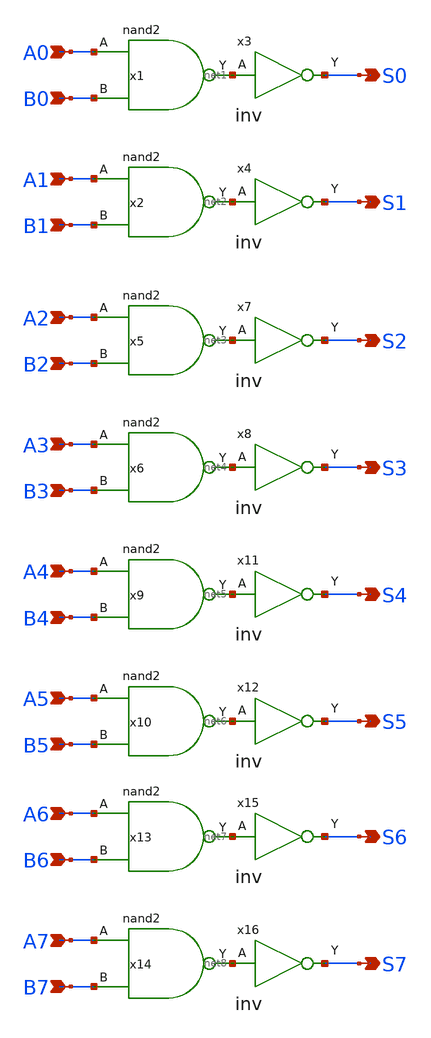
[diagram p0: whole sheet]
** sch_path: design/xschem/NAND/nand_8_bitwise.sch
**.subckt nand_8_bitwise S0 S1 S2 S3 S4 S5 S6 S7 A0 B0 A1 B1 A2 B2 A3 B3 A4 B4 A5 B5 A6 B6 A7 B7
*.opin S0
*.opin S1
*.opin S2
*.opin S3
*.opin S4
*.opin S5
*.opin S6
*.opin S7
*.ipin A0
*.ipin B0
*.ipin A1
*.ipin B1
*.ipin A2
*.ipin B2
*.ipin A3
*.ipin B3
*.ipin A4
*.ipin B4
*.ipin A5
*.ipin B5
*.ipin A6
*.ipin B6
*.ipin A7
*.ipin B7
x1 A0 B0 VSS VDD net1 nand2
x2 A1 B1 VSS VDD net2 nand2
x3 net1 VSS VDD S0 inv
x4 net2 VSS VDD S1 inv
x5 A2 B2 VSS VDD net3 nand2
x6 A3 B3 VSS VDD net4 nand2
x7 net3 VSS VDD S2 inv
x8 net4 VSS VDD S3 inv
x9 A4 B4 VSS VDD net5 nand2
x10 A5 B5 VSS VDD net6 nand2
x11 net5 VSS VDD S4 inv
x12 net6 VSS VDD S5 inv
x13 A6 B6 VSS VDD net7 nand2
x14 A7 B7 VSS VDD net8 nand2
x15 net7 VSS VDD S6 inv
x16 net8 VSS VDD S7 inv
**.ends

* expanding   symbol:  NAND/nand2.sym # of pins=3
** sym_path: design/xschem/NAND/nand2.sym
** sch_path: design/xschem/NAND/nand2.sch
.subckt nand2 A B VSS VDD Y
*.ipin A
*.opin Y
*.ipin B
XM1 Y A VDD VDD sky130_fd_pr__pfet_01v8 L=0.15 W=3.2 nf=1 ad='int((nf+1)/2) * W/nf * 0.29' as='int((nf+2)/2) * W/nf * 0.29'
+ pd='2*int((nf+1)/2) * (W/nf + 0.29)' ps='2*int((nf+2)/2) * (W/nf + 0.29)' nrd='0.29 / W' nrs='0.29 / W'
+ sa=0 sb=0 sd=0 mult=1 m=1
XM2 Y A net1 net1 sky130_fd_pr__nfet_01v8 L=0.15 W=2 nf=1 ad='int((nf+1)/2) * W/nf * 0.29' as='int((nf+2)/2) * W/nf * 0.29'
+ pd='2*int((nf+1)/2) * (W/nf + 0.29)' ps='2*int((nf+2)/2) * (W/nf + 0.29)' nrd='0.29 / W' nrs='0.29 / W'
+ sa=0 sb=0 sd=0 mult=1 m=1
XM3 net1 B VSS VSS sky130_fd_pr__nfet_01v8 L=0.15 W=2 nf=1 ad='int((nf+1)/2) * W/nf * 0.29' as='int((nf+2)/2) * W/nf * 0.29'
+ pd='2*int((nf+1)/2) * (W/nf + 0.29)' ps='2*int((nf+2)/2) * (W/nf + 0.29)' nrd='0.29 / W' nrs='0.29 / W'
+ sa=0 sb=0 sd=0 mult=1 m=1
XM4 Y B VDD VDD sky130_fd_pr__pfet_01v8 L=0.15 W=3.2 nf=1 ad='int((nf+1)/2) * W/nf * 0.29' as='int((nf+2)/2) * W/nf * 0.29'
+ pd='2*int((nf+1)/2) * (W/nf + 0.29)' ps='2*int((nf+2)/2) * (W/nf + 0.29)' nrd='0.29 / W' nrs='0.29 / W'
+ sa=0 sb=0 sd=0 mult=1 m=1
.ends


* expanding   symbol:  INV/inv.sym # of pins=2
** sym_path: design/xschem/INV/inv.sym
** sch_path: design/xschem/INV/inv.sch
.subckt inv A VSS VDD Y
*.ipin A
*.opin Y
XM2 Y A VSS GND sky130_fd_pr__nfet_01v8 L=0.15 W=1 nf=1 ad='int((nf+1)/2) * W/nf * 0.29' as='int((nf+2)/2) * W/nf * 0.29'
+ pd='2*int((nf+1)/2) * (W/nf + 0.29)' ps='2*int((nf+2)/2) * (W/nf + 0.29)' nrd='0.29 / W' nrs='0.29 / W'
+ sa=0 sb=0 sd=0 mult=1 m=1
XM1 Y A VDD VDD sky130_fd_pr__pfet_01v8 L=0.15 W=3.21 nf=1 ad='int((nf+1)/2) * W/nf * 0.29' as='int((nf+2)/2) * W/nf * 0.29'
+ pd='2*int((nf+1)/2) * (W/nf + 0.29)' ps='2*int((nf+2)/2) * (W/nf + 0.29)' nrd='0.29 / W' nrs='0.29 / W'
+ sa=0 sb=0 sd=0 mult=1 m=1
.ends

.end
